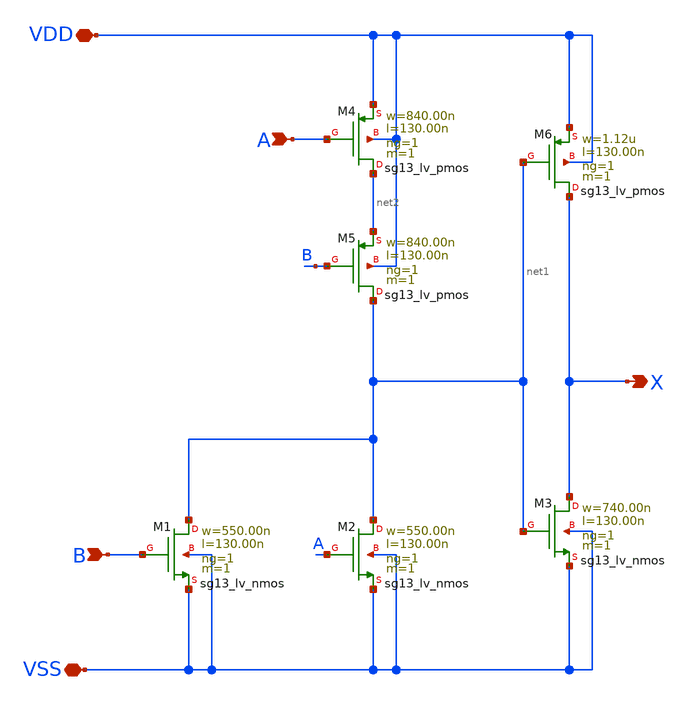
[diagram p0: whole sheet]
** sch_path: ihp-sg13g2/libs.tech/xschem/sg13g2_stdcells/sg13g2_or2_1.sch
**.subckt sg13g2_or2_1 X B A VDD VSS
*.opin X
*.ipin B
*.ipin A
*.iopin VDD
*.iopin VSS
XM1 net1 B VSS VSS sg13_lv_nmos w=550.00n l=130.00n ng=1 m=1 mm_ok=1
XM2 net1 A VSS VSS sg13_lv_nmos w=550.00n l=130.00n ng=1 m=1 mm_ok=1
XM3 X net1 VSS VSS sg13_lv_nmos w=740.00n l=130.00n ng=1 m=1 mm_ok=1
XM4 net2 A VDD VDD sg13_lv_pmos w=840.00n l=130.00n ng=1 m=1 mm_ok=1
XM5 net1 B net2 VDD sg13_lv_pmos w=840.00n l=130.00n ng=1 m=1 mm_ok=1
XM6 X net1 VDD VDD sg13_lv_pmos w=1.12u l=130.00n ng=1 m=1 mm_ok=1
**.ends
.end
